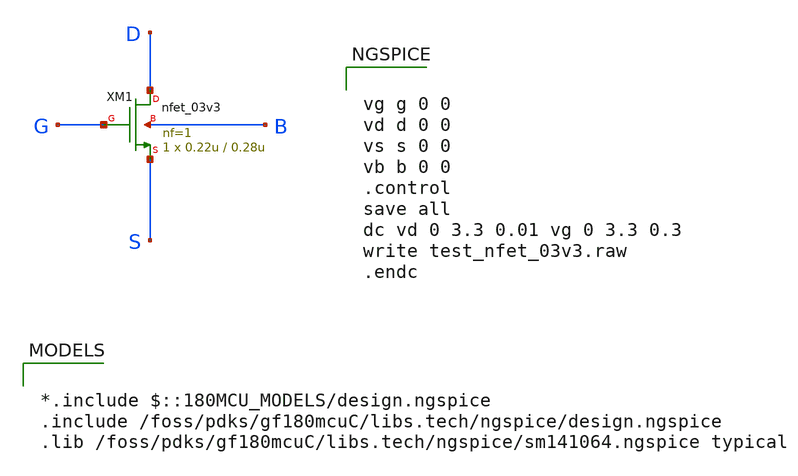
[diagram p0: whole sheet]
** sch_path: designs/analog_test/test_nfet_03v3.sch
* Copyright 2022 GlobalFoundries PDK Authors
* Licensed under the Apache License, Version 2.0 (the "License");
* you may not use this file except in compliance with the License.
* You may obtain a copy of the License at
* https://www.apache.org/licenses/LICENSE-2.0
* Unless required by applicable law or agreed to in writing, software
* distributed under the License is distributed on an "AS IS" BASIS,
* WITHOUT WARRANTIES OR CONDITIONS OF ANY KIND, either express or implied.
* See the License for the specific language governing permissions and
* limitations under the License.
**.subckt test_nfet_03v3
XM1 D G S B nfet_03v3 L=0.28u W=0.22u nf=1 ad='int((nf+1)/2) * W/nf * 0.18u' as='int((nf+2)/2) * W/nf * 0.18u'
+ pd='2*int((nf+1)/2) * (W/nf + 0.18u)' ps='2*int((nf+2)/2) * (W/nf + 0.18u)' nrd='0.18u / W' nrs='0.18u / W'
+ sa=0 sb=0 sd=0 m=1
**** begin user architecture code

*.include $::180MCU_MODELS/design.ngspice
.include /foss/pdks/gf180mcuC/libs.tech/ngspice/design.ngspice
.lib /foss/pdks/gf180mcuC/libs.tech/ngspice/sm141064.ngspice typical



vg g 0 0
vd d 0 0
vs s 0 0
vb b 0 0
.control
save all
dc vd 0 3.3 0.01 vg 0 3.3 0.3
write test_nfet_03v3.raw
.endc


**** end user architecture code
**.ends
.end
